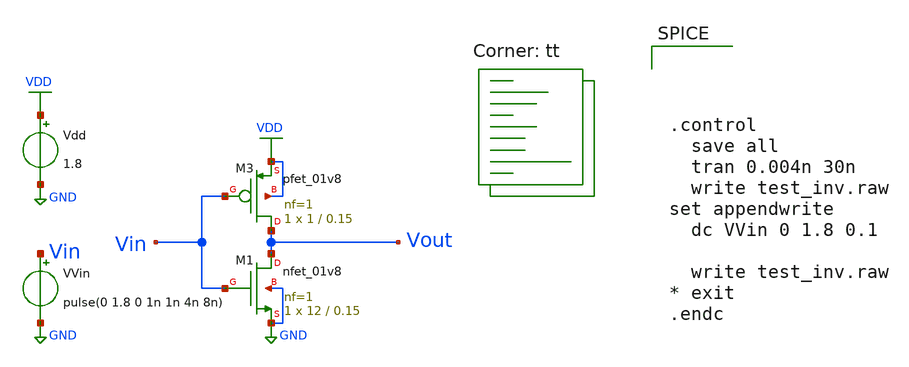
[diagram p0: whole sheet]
** sch_path: cmos_inverter.sch
**.subckt cmos_inverter
Vdd VDD GND 1.8
VVin Vin GND pulse(0 1.8 0 1n 1n 4n 8n)
XM3 Vout Vin VDD VDD sky130_fd_pr__pfet_01v8 L=0.15 W=1 nf=1 ad='int((nf+1)/2) * W/nf * 0.29' as='int((nf+2)/2) * W/nf * 0.29'
+ pd='2*int((nf+1)/2) * (W/nf + 0.29)' ps='2*int((nf+2)/2) * (W/nf + 0.29)' nrd='0.29 / W' nrs='0.29 / W'
+ sa=0 sb=0 sd=0 mult=1 m=1
XM1 Vout Vin GND GND sky130_fd_pr__nfet_01v8 L=0.15 W=12 nf=1 ad='int((nf+1)/2) * W/nf * 0.29' as='int((nf+2)/2) * W/nf * 0.29'
+ pd='2*int((nf+1)/2) * (W/nf + 0.29)' ps='2*int((nf+2)/2) * (W/nf + 0.29)' nrd='0.29 / W' nrs='0.29 / W'
+ sa=0 sb=0 sd=0 mult=1 m=1
**** begin user architecture code
.lib $::SKYWATER_MODELS/sky130.lib.spice tt




.control
  save all
  tran 0.004n 30n
  write test_inv.raw
set appendwrite
  dc VVin 0 1.8 0.1

  write test_inv.raw
* exit
.endc


**** end user architecture code
**.ends
.GLOBAL VDD
.GLOBAL GND
.end
